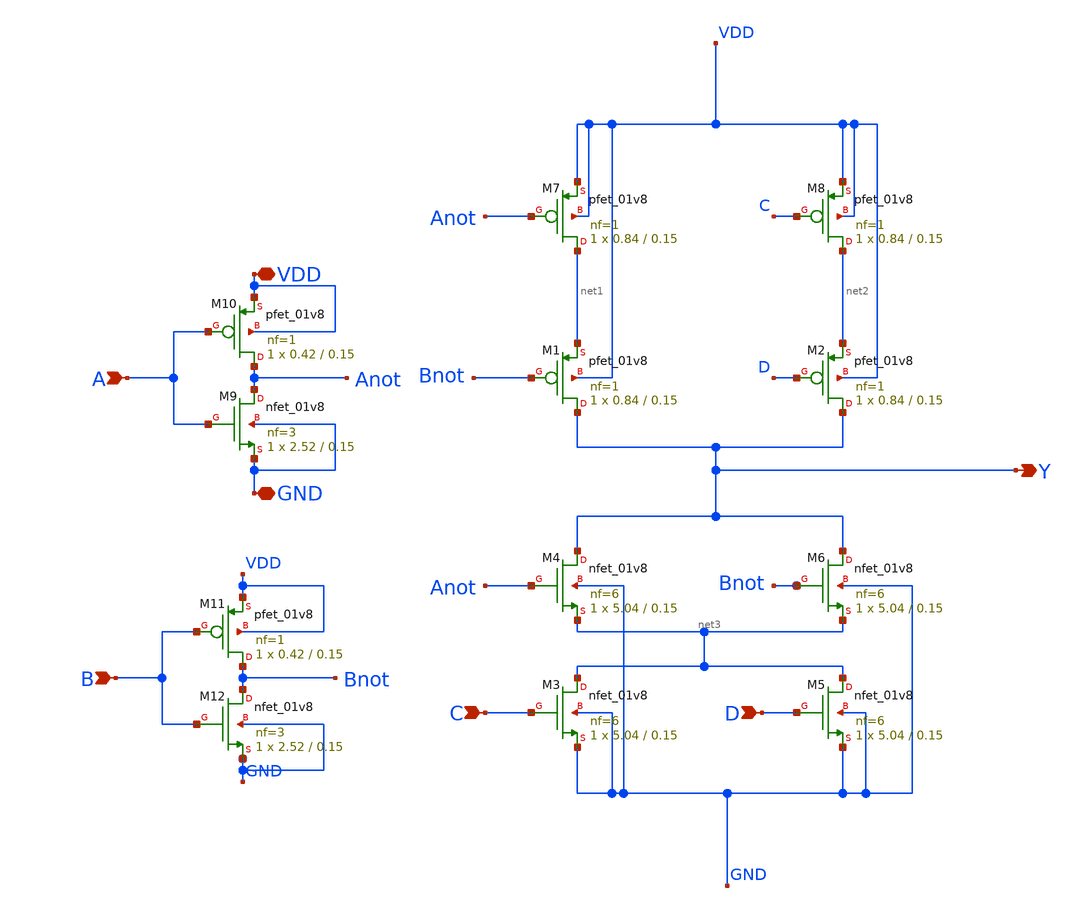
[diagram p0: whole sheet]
** sch_path: cells/MOAI4X1/schematic/moai4x1.sch
**.subckt moai4x1 A VDD GND B D C Y
*.ipin A
*.iopin VDD
*.iopin GND
*.ipin B
*.ipin D
*.ipin C
*.opin Y
XM9 Anot A GND GND sky130_fd_pr__nfet_01v8 L=0.15 W=2.52 nf=3 ad='int((3 + 1)/2) * 2.52 / 3 * 0.29' as='int((3 + 2)/2) * 2.52 / 3 * 0.29'
+ pd='2*int((3 + 1)/2) * (2.52 / 3 + 0.29)' ps='2*int((3 + 2)/2) * (2.52 / 3 + 0.29)' nrd='0.29 / 2.52 '
+ nrs='0.29 / 2.52 ' sa=0 sb=0 sd=0 mult=1 m=1
XM10 Anot A VDD VDD sky130_fd_pr__pfet_01v8 L=0.15 W=0.42 nf=1 ad='int((1 + 1)/2) * 0.42 / 1 * 0.29'
+ as='int((1 + 2)/2) * 0.42 / 1 * 0.29' pd='2*int((1 + 1)/2) * (0.42 / 1 + 0.29)' ps='2*int((1 + 2)/2) * (0.42 / 1 + 0.29)'
+ nrd='0.29 / 0.42 ' nrs='0.29 / 0.42 ' sa=0 sb=0 sd=0 mult=1 m=1
XM4 Y Anot net3 GND sky130_fd_pr__nfet_01v8 L=0.15 W=5.04 nf=6 ad='int((6 + 1)/2) * 5.04 / 6 * 0.29'
+ as='int((6 + 2)/2) * 5.04 / 6 * 0.29' pd='2*int((6 + 1)/2) * (5.04 / 6 + 0.29)' ps='2*int((6 + 2)/2) * (5.04 / 6 + 0.29)'
+ nrd='0.29 / 5.04 ' nrs='0.29 / 5.04 ' sa=0 sb=0 sd=0 mult=1 m=1
XM7 net1 Anot VDD VDD sky130_fd_pr__pfet_01v8 L=0.15 W=0.84 nf=1 ad='int((1 + 1)/2) * 0.84 / 1 * 0.29'
+ as='int((1 + 2)/2) * 0.84 / 1 * 0.29' pd='2*int((1 + 1)/2) * (0.84 / 1 + 0.29)' ps='2*int((1 + 2)/2) * (0.84 / 1 + 0.29)'
+ nrd='0.29 / 0.84 ' nrs='0.29 / 0.84 ' sa=0 sb=0 sd=0 mult=1 m=1
XM1 Y Bnot net1 VDD sky130_fd_pr__pfet_01v8 L=0.15 W=0.84 nf=1 ad='int((1 + 1)/2) * 0.84 / 1 * 0.29'
+ as='int((1 + 2)/2) * 0.84 / 1 * 0.29' pd='2*int((1 + 1)/2) * (0.84 / 1 + 0.29)' ps='2*int((1 + 2)/2) * (0.84 / 1 + 0.29)'
+ nrd='0.29 / 0.84 ' nrs='0.29 / 0.84 ' sa=0 sb=0 sd=0 mult=1 m=1
XM2 Y D net2 VDD sky130_fd_pr__pfet_01v8 L=0.15 W=0.84 nf=1 ad='int((1 + 1)/2) * 0.84 / 1 * 0.29' as='int((1 + 2)/2) * 0.84 / 1 * 0.29'
+ pd='2*int((1 + 1)/2) * (0.84 / 1 + 0.29)' ps='2*int((1 + 2)/2) * (0.84 / 1 + 0.29)' nrd='0.29 / 0.84 '
+ nrs='0.29 / 0.84 ' sa=0 sb=0 sd=0 mult=1 m=1
XM8 net2 C VDD VDD sky130_fd_pr__pfet_01v8 L=0.15 W=0.84 nf=1 ad='int((1 + 1)/2) * 0.84 / 1 * 0.29' as='int((1 + 2)/2) * 0.84 / 1 * 0.29'
+ pd='2*int((1 + 1)/2) * (0.84 / 1 + 0.29)' ps='2*int((1 + 2)/2) * (0.84 / 1 + 0.29)' nrd='0.29 / 0.84 '
+ nrs='0.29 / 0.84 ' sa=0 sb=0 sd=0 mult=1 m=1
XM11 Bnot B VDD VDD sky130_fd_pr__pfet_01v8 L=0.15 W=0.42 nf=1 ad='int((1 + 1)/2) * 0.42 / 1 * 0.29'
+ as='int((1 + 2)/2) * 0.42 / 1 * 0.29' pd='2*int((1 + 1)/2) * (0.42 / 1 + 0.29)' ps='2*int((1 + 2)/2) * (0.42 / 1 + 0.29)'
+ nrd='0.29 / 0.42 ' nrs='0.29 / 0.42 ' sa=0 sb=0 sd=0 mult=1 m=1
XM12 Bnot B GND GND sky130_fd_pr__nfet_01v8 L=0.15 W=2.52 nf=3 ad='int((3 + 1)/2) * 2.52 / 3 * 0.29'
+ as='int((3 + 2)/2) * 2.52 / 3 * 0.29' pd='2*int((3 + 1)/2) * (2.52 / 3 + 0.29)' ps='2*int((3 + 2)/2) * (2.52 / 3 + 0.29)'
+ nrd='0.29 / 2.52 ' nrs='0.29 / 2.52 ' sa=0 sb=0 sd=0 mult=1 m=1
XM3 net3 C GND GND sky130_fd_pr__nfet_01v8 L=0.15 W=5.04 nf=6 ad='int((6 + 1)/2) * 5.04 / 6 * 0.29' as='int((6 + 2)/2) * 5.04 / 6 * 0.29'
+ pd='2*int((6 + 1)/2) * (5.04 / 6 + 0.29)' ps='2*int((6 + 2)/2) * (5.04 / 6 + 0.29)' nrd='0.29 / 5.04 '
+ nrs='0.29 / 5.04 ' sa=0 sb=0 sd=0 mult=1 m=1
XM5 net3 D GND GND sky130_fd_pr__nfet_01v8 L=0.15 W=5.04 nf=6 ad='int((6 + 1)/2) * 5.04 / 6 * 0.29' as='int((6 + 2)/2) * 5.04 / 6 * 0.29'
+ pd='2*int((6 + 1)/2) * (5.04 / 6 + 0.29)' ps='2*int((6 + 2)/2) * (5.04 / 6 + 0.29)' nrd='0.29 / 5.04 '
+ nrs='0.29 / 5.04 ' sa=0 sb=0 sd=0 mult=1 m=1
XM6 Y Bnot net3 GND sky130_fd_pr__nfet_01v8 L=0.15 W=5.04 nf=6 ad='int((6 + 1)/2) * 5.04 / 6 * 0.29'
+ as='int((6 + 2)/2) * 5.04 / 6 * 0.29' pd='2*int((6 + 1)/2) * (5.04 / 6 + 0.29)' ps='2*int((6 + 2)/2) * (5.04 / 6 + 0.29)'
+ nrd='0.29 / 5.04 ' nrs='0.29 / 5.04 ' sa=0 sb=0 sd=0 mult=1 m=1
**.ends
.end
